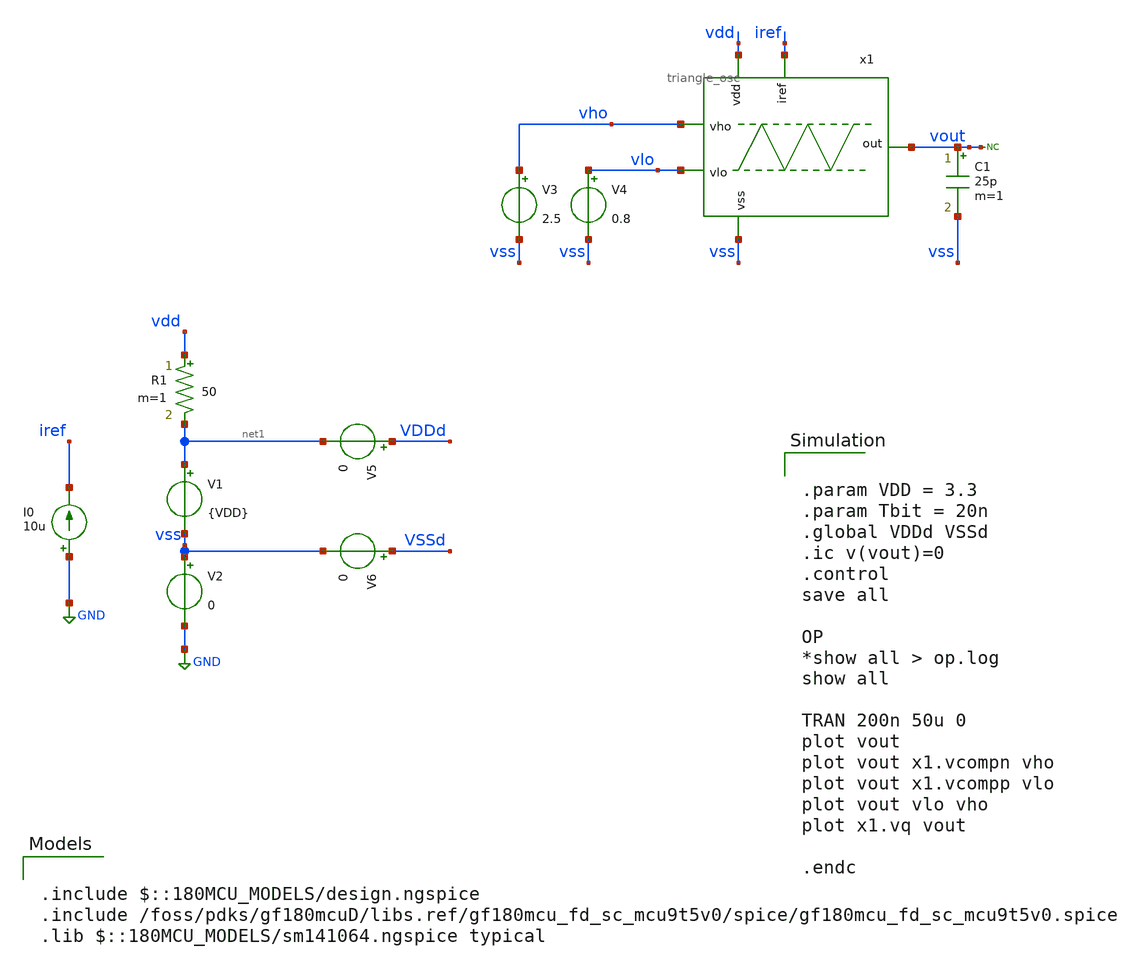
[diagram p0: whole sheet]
** sch_path: designs/switch_matrix_gf180mcu_9t5v0-main/designs/libs/tb_analog/oscillator/test_oscillator.sch
**.subckt test_oscillator
x1 vdd vho vout vlo iref vss triangle_osc
V1 net1 vss {VDD}
V2 vss GND 0
V3 vho vss 2.5
V4 vlo vss 0.8
I0 GND iref 10u
* noconn vout
C1 vout vss 25p m=1
V5 VDDd net1 0
V6 VSSd vss 0
R1 vdd net1 50 m=1
**** begin user architecture code

.include $::180MCU_MODELS/design.ngspice
.include /foss/pdks/gf180mcuD/libs.ref/gf180mcu_fd_sc_mcu9t5v0/spice/gf180mcu_fd_sc_mcu9t5v0.spice
.lib $::180MCU_MODELS/sm141064.ngspice typical



.param VDD = 3.3
.param Tbit = 20n
.global VDDd VSSd
.ic v(vout)=0
.control
save all

OP
*show all > op.log
show all

TRAN 200n 50u 0
plot vout
plot vout x1.vcompn vho
plot vout x1.vcompp vlo
plot vout vlo vho
plot x1.vq vout

.endc


**** end user architecture code
**.ends
.GLOBAL GND
.end
